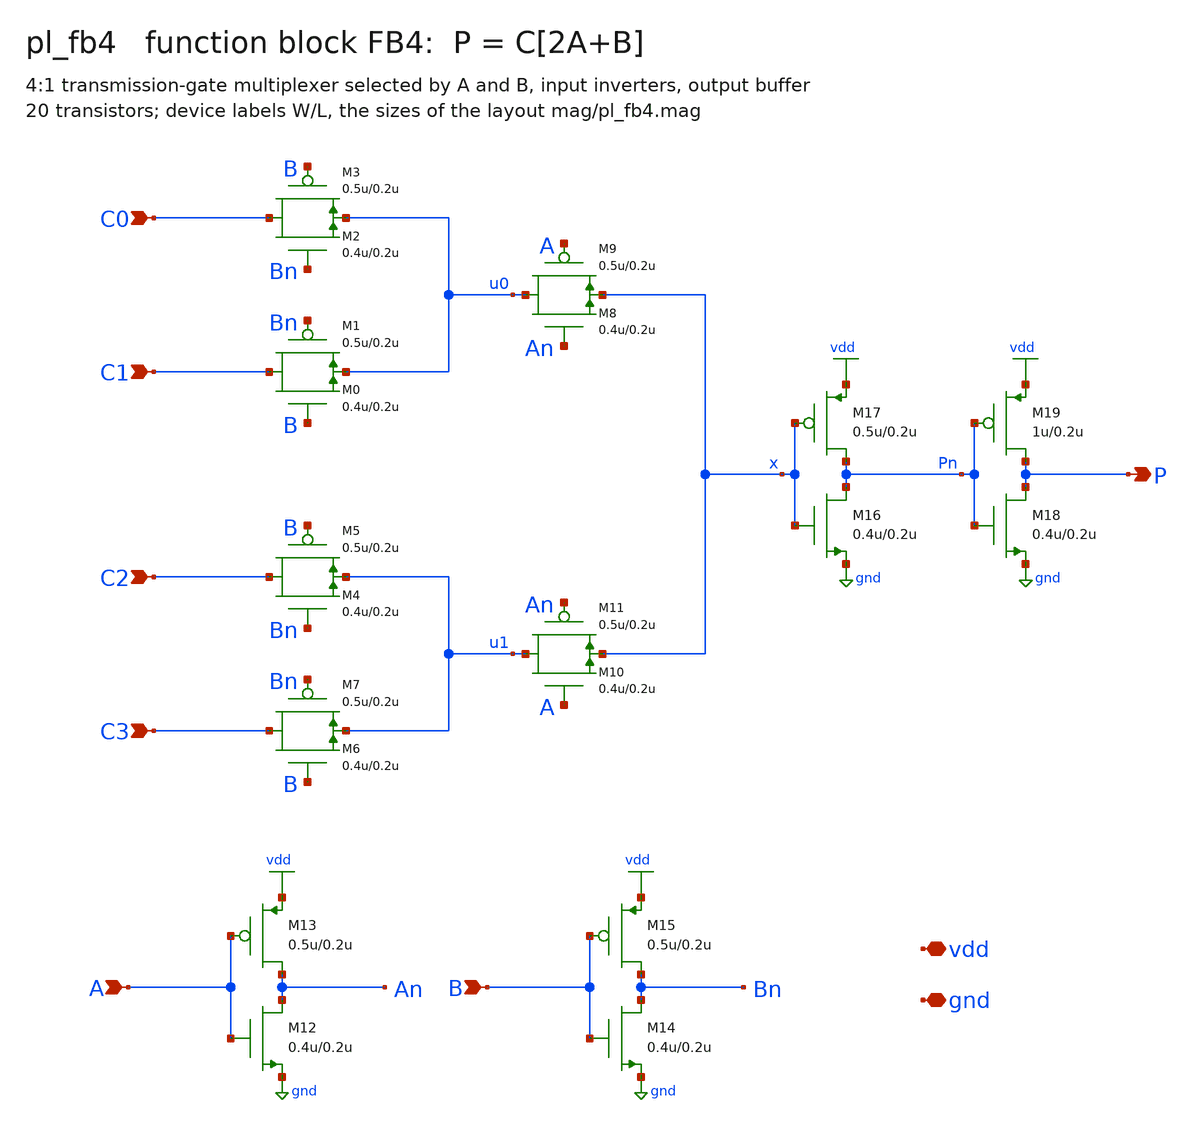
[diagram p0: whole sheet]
** sch_path: demo/xschem/pl_fb4.sch
**.subckt pl_fb4 C0 C1 C2 C3 P A B vdd gnd
*.ipin C0
*.ipin C1
*.ipin C2
*.ipin C3
*.opin P
*.ipin A
*.ipin B
*.iopin vdd
*.iopin gnd
M3 C0 B u0 vdd pfet w=0.5u l=0.2u m=1
M2 C0 Bn u0 gnd nfet w=0.4u l=0.2u m=1
M1 C1 Bn u0 vdd pfet w=0.5u l=0.2u m=1
M0 C1 B u0 gnd nfet w=0.4u l=0.2u m=1
M5 C2 B u1 vdd pfet w=0.5u l=0.2u m=1
M4 C2 Bn u1 gnd nfet w=0.4u l=0.2u m=1
M7 C3 Bn u1 vdd pfet w=0.5u l=0.2u m=1
M6 C3 B u1 gnd nfet w=0.4u l=0.2u m=1
M9 u0 A x vdd pfet w=0.5u l=0.2u m=1
M8 u0 An x gnd nfet w=0.4u l=0.2u m=1
M11 u1 An x vdd pfet w=0.5u l=0.2u m=1
M10 u1 A x gnd nfet w=0.4u l=0.2u m=1
M17 Pn x vdd vdd pfet w=0.5u l=0.2u m=1
M16 Pn x gnd gnd nfet w=0.4u l=0.2u m=1
M19 P Pn vdd vdd pfet w=1u l=0.2u m=1
M18 P Pn gnd gnd nfet w=0.4u l=0.2u m=1
M13 An A vdd vdd pfet w=0.5u l=0.2u m=1
M12 An A gnd gnd nfet w=0.4u l=0.2u m=1
M15 Bn B vdd vdd pfet w=0.5u l=0.2u m=1
M14 Bn B gnd gnd nfet w=0.4u l=0.2u m=1
**.ends
.GLOBAL vdd
.GLOBAL gnd
.end
